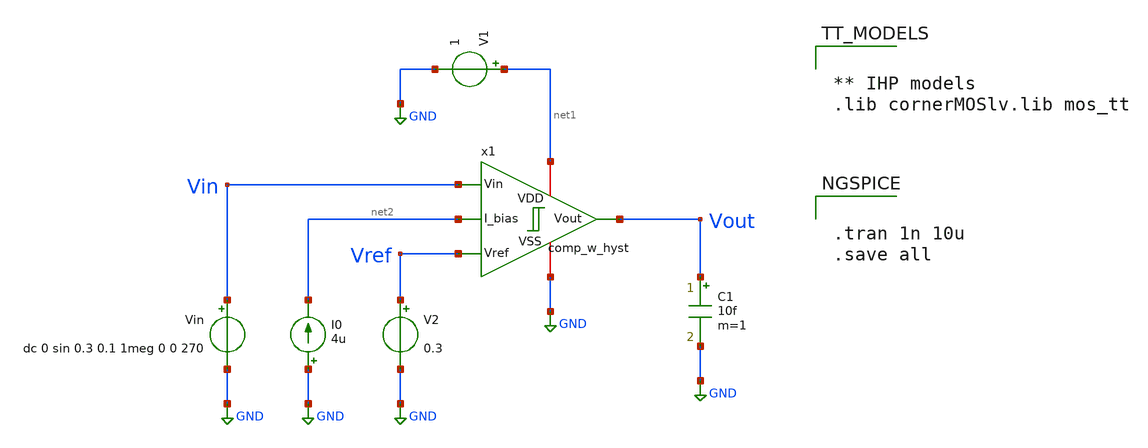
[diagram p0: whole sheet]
** sch_path: SSDOR_1.2V_v3/components/comp_w_hyst/tb_comp_w_hyst.sch
**.subckt tb_comp_w_hyst
V1 net1 GND 1
C1 Vout GND 10f m=1
V2 Vref GND 0.3
I0 GND net2 4u
Vin Vin GND dc 0 sin 0.3 0.1 1meg 0 0 270
x1 net1 GND Vref Vin Vout net2 comp_w_hyst
**** begin user architecture code


** IHP models
.lib cornerMOSlv.lib mos_tt




.tran 1n 10u
.save all


**** end user architecture code
**.ends
.GLOBAL GND
.end
